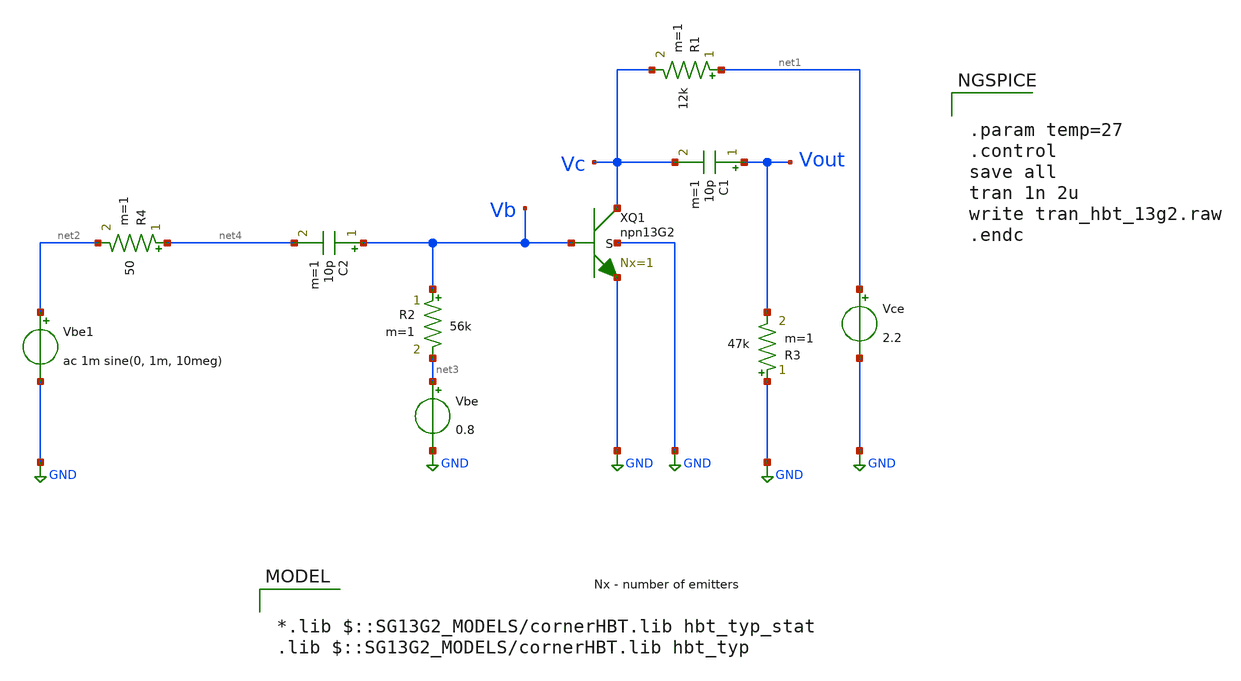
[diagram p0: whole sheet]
** sch_path: ihp-sg13g2/libs.tech/xschem/sg13g2_tests/tran_hbt_13g2.sch
* Copyright 2023 IHP PDK Authors
**.subckt tran_hbt_13g2
Vce net1 GND 2.2
XQ1 Vc Vb GND GND npn13G2 Nx=1
R1 net1 Vc 12k m=1
Vbe1 net2 GND ac 1m sine(0, 1m, 10meg)
R2 Vb net3 56k m=1
Vbe net3 GND 0.8
R3 GND Vout 47k m=1
C1 Vout Vc 10p m=1
C2 Vb net4 10p m=1
R4 net4 net2 50 m=1
**** begin user architecture code

*.lib $::SG13G2_MODELS/cornerHBT.lib hbt_typ_stat
.lib $::SG13G2_MODELS/cornerHBT.lib hbt_typ



.param temp=27
.control
save all
tran 1n 2u
write tran_hbt_13g2.raw
.endc


**** end user architecture code
**.ends
.GLOBAL GND
.end
